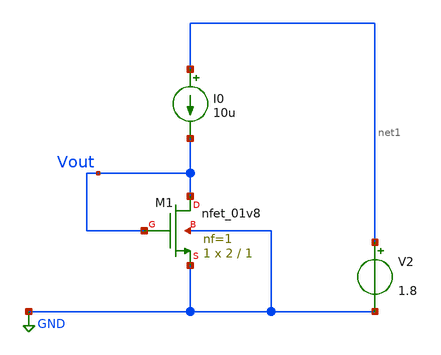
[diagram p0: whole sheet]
** sch_path: xschem/misc/testing/loop2.sch
**.subckt loop2
XM1 Vout Vout GND GND sky130_fd_pr__nfet_01v8 L=1 W=2 nf=1 ad='int((nf+1)/2) * W/nf * 0.29' as='int((nf+2)/2) * W/nf * 0.29'
+ pd='2*int((nf+1)/2) * (W/nf + 0.29)' ps='2*int((nf+2)/2) * (W/nf + 0.29)' nrd='0.29 / W' nrs='0.29 / W'
+ sa=0 sb=0 sd=0 mult=1 m=1
I0 net1 Vout 10u
V2 net1 GND 1.8
**** begin user architecture code

** opencircuitdesign pdks install
.lib $::SKYWATER_MODELS/sky130.lib.spice tt




.options savecurrents

*** plot temperature coefficient
*Vdd VDD GND 3.3
*V_en en GND 3.3
*.dc temp -40 140 1
.control
save all
run
dc temp -40 100 1
plot Vout




.endc



*** plot voltage coefficient
*Vdd VDD GND 3.3
*V_en en GND 3.3
*.dc Vdd 2 4 0.1
*.control
*run
*plot deriv(V(Vbgp))
*.endc

*** plot temperature coefficient
*Vdd VDD GND 3.3
*V_en en GND 3.3
*.dc temp -40 140 1
*.control
*run
*plot deriv(V(Vbgp))/1.202344
*.endc



*** enable pin
*Vdd VDD GND 3.3
*V_en en GND PULSE(0 3.3 0 200us 200us 600us 2000us 0)
*.tran 1u 2000us
*.control
*run
*plot V(en)
*plot -I(VDD)
*.endc


**** end user architecture code
**.ends
.GLOBAL GND
.end
